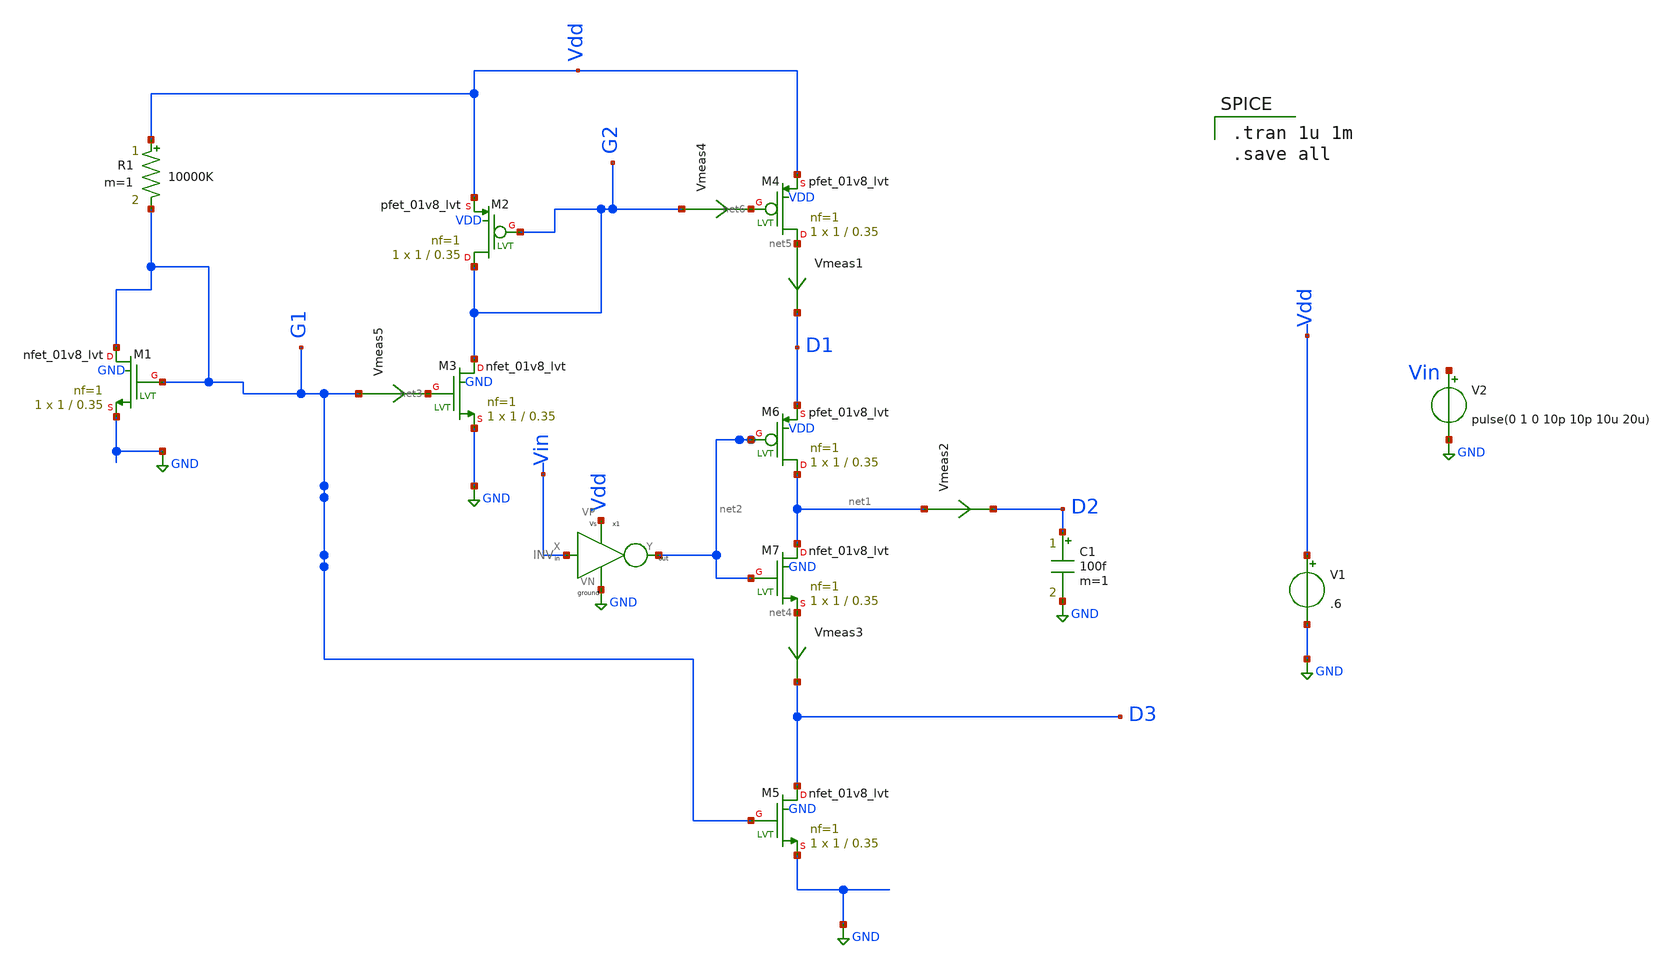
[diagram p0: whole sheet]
** sch_path: component/current_mirror/current_source.sch
**.subckt current_source
R1 Vdd G1 10000K m=1
V1 Vdd GND .6
C1 D2 GND 100f m=1
V2 Vin GND pulse(0 1 0 10p 10p 10u 20u)
XM1 G1 G1 GND GND sky130_fd_pr__nfet_01v8_lvt L=0.35 W=1 nf=1 ad='int((nf+1)/2) * W/nf * 0.29' as='int((nf+2)/2) * W/nf * 0.29'
+ pd='2*int((nf+1)/2) * (W/nf + 0.29)' ps='2*int((nf+2)/2) * (W/nf + 0.29)' nrd='0.29 / W' nrs='0.29 / W'
+ sa=0 sb=0 sd=0 mult=1 m=1
XM3 G2 net3 GND GND sky130_fd_pr__nfet_01v8_lvt L=0.35 W=1 nf=1 ad='int((nf+1)/2) * W/nf * 0.29' as='int((nf+2)/2) * W/nf * 0.29'
+ pd='2*int((nf+1)/2) * (W/nf + 0.29)' ps='2*int((nf+2)/2) * (W/nf + 0.29)' nrd='0.29 / W' nrs='0.29 / W'
+ sa=0 sb=0 sd=0 mult=1 m=1
XM7 net1 net2 net4 GND sky130_fd_pr__nfet_01v8_lvt L=0.35 W=1 nf=1 ad='int((nf+1)/2) * W/nf * 0.29' as='int((nf+2)/2) * W/nf * 0.29'
+ pd='2*int((nf+1)/2) * (W/nf + 0.29)' ps='2*int((nf+2)/2) * (W/nf + 0.29)' nrd='0.29 / W' nrs='0.29 / W'
+ sa=0 sb=0 sd=0 mult=1 m=1
XM5 D3 G1 GND GND sky130_fd_pr__nfet_01v8_lvt L=0.35 W=1 nf=1 ad='int((nf+1)/2) * W/nf * 0.29' as='int((nf+2)/2) * W/nf * 0.29'
+ pd='2*int((nf+1)/2) * (W/nf + 0.29)' ps='2*int((nf+2)/2) * (W/nf + 0.29)' nrd='0.29 / W' nrs='0.29 / W'
+ sa=0 sb=0 sd=0 mult=1 m=1
XM2 G2 G2 Vdd VDD sky130_fd_pr__pfet_01v8_lvt L=0.35 W=1 nf=1 ad='int((nf+1)/2) * W/nf * 0.29' as='int((nf+2)/2) * W/nf * 0.29'
+ pd='2*int((nf+1)/2) * (W/nf + 0.29)' ps='2*int((nf+2)/2) * (W/nf + 0.29)' nrd='0.29 / W' nrs='0.29 / W'
+ sa=0 sb=0 sd=0 mult=1 m=1
XM4 net5 net6 Vdd VDD sky130_fd_pr__pfet_01v8_lvt L=0.35 W=1 nf=1 ad='int((nf+1)/2) * W/nf * 0.29' as='int((nf+2)/2) * W/nf * 0.29'
+ pd='2*int((nf+1)/2) * (W/nf + 0.29)' ps='2*int((nf+2)/2) * (W/nf + 0.29)' nrd='0.29 / W' nrs='0.29 / W'
+ sa=0 sb=0 sd=0 mult=1 m=1
XM6 net1 net2 D1 VDD sky130_fd_pr__pfet_01v8_lvt L=0.35 W=1 nf=1 ad='int((nf+1)/2) * W/nf * 0.29' as='int((nf+2)/2) * W/nf * 0.29'
+ pd='2*int((nf+1)/2) * (W/nf + 0.29)' ps='2*int((nf+2)/2) * (W/nf + 0.29)' nrd='0.29 / W' nrs='0.29 / W'
+ sa=0 sb=0 sd=0 mult=1 m=1
Vmeas1 net5 D1 0
.save i(vmeas1)
Vmeas2 net1 D2 0
.save i(vmeas2)
Vmeas3 net4 D3 0
.save i(vmeas3)
Vmeas4 G2 net6 0
.save i(vmeas4)
Vmeas5 G1 net3 0
.save i(vmeas5)
x1 Vin net2 Vdd GND INV
**** begin user architecture code

** opencircuitdesign pdks install
.lib $::SKYWATER_MODELS/sky130.lib.spice tt



.tran 1u 1m
.save all

**** end user architecture code
**.ends

* expanding   symbol:  component/INV/INV.sym # of pins=4
** sym_path: component/INV/INV.sym
** sch_path: component/INV/INV.sch
.subckt INV X Y VP VN
*.ipin X
*.opin Y
*.iopin VN
*.iopin VP
XM1 Y X VN VN sky130_fd_pr__nfet_01v8 L=0.15 W=0.42 nf=1 ad='int((nf+1)/2) * W/nf * 0.29' as='int((nf+2)/2) * W/nf * 0.29'
+ pd='2*int((nf+1)/2) * (W/nf + 0.29)' ps='2*int((nf+2)/2) * (W/nf + 0.29)' nrd='0.29 / W' nrs='0.29 / W'
+ sa=0 sb=0 sd=0 mult=1 m=1
XM2 Y X VP VP sky130_fd_pr__pfet_01v8 L=0.15 W=1.26 nf=1 ad='int((nf+1)/2) * W/nf * 0.29' as='int((nf+2)/2) * W/nf * 0.29'
+ pd='2*int((nf+1)/2) * (W/nf + 0.29)' ps='2*int((nf+2)/2) * (W/nf + 0.29)' nrd='0.29 / W' nrs='0.29 / W'
+ sa=0 sb=0 sd=0 mult=1 m=1
.ends

.GLOBAL GND
.end
